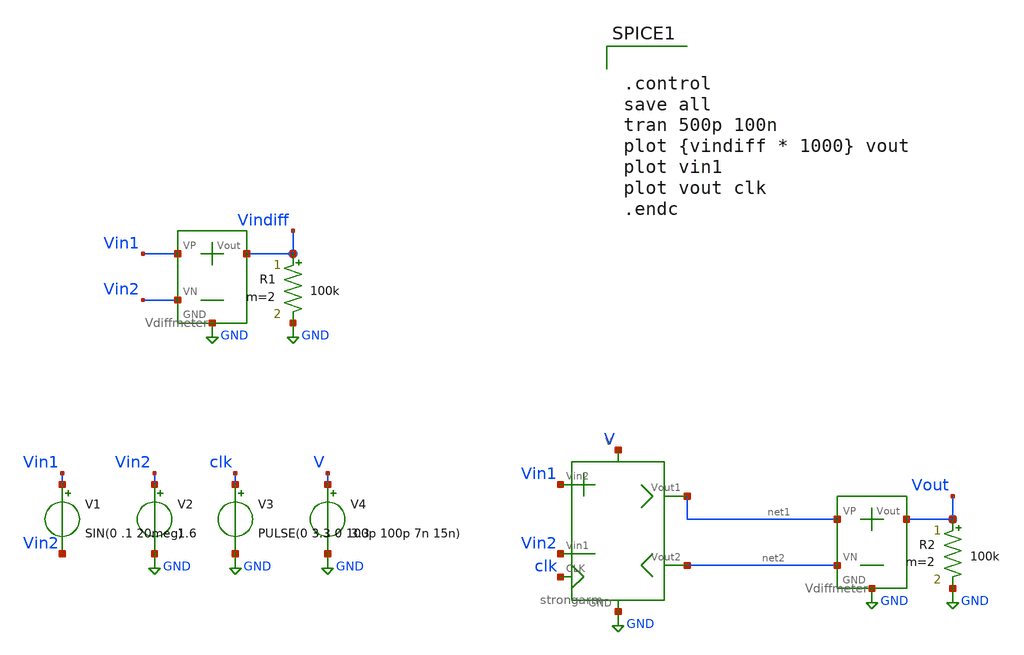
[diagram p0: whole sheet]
** sch_path: SAR_ADC/xschem/test/strongarm_tb/sin_1m__tb.sch
**.subckt sin_1m__tb
V1 Vin1 Vin2 SIN(0 .1 20meg)
V2 Vin2 GND 1.6
V3 clk GND PULSE(0 3.3 0 100p 100p 7n 15n)
V4 V GND 3.3
R1 Vindiff GND 100k m=2
R2 Vout GND 100k m=2
X1 V GND Vin2 Vin1 clk net1 net2 strongarm
X3 net1 net2 Vout GND Vdiffmeter
X2 Vin1 Vin2 Vindiff GND Vdiffmeter
**** begin user architecture code


.control
save all
tran 500p 100n
plot {vindiff * 1000} vout
plot vin1
plot vout clk
.endc


.include $::PDK_ROOT/gf180mcuC/libs.tech/ngspice/design.ngspice
.lib $::PDK_ROOT/gf180mcuC/libs.tech/ngspice/sm141064.ngspice typical

**** end user architecture code
**.ends

* expanding   symbol:  ../../../symbols/strongarm.sym # of pins=7
** sym_path: SAR_ADC/xschem/designs/strongarm.sym
** sch_path: SAR_ADC/xschem/designs/strongarm.sch
.subckt strongarm V GND Vin1 Vin2 CLK Vout1 Vout2
*.iopin V
*.iopin Vout1
*.iopin Vin1
*.iopin Vin2
*.iopin Vout2
*.iopin CLK
*.iopin GND
XM1 net3 Vout2 V V pfet_03v3 L=0.28u W=2u nf=1 ad='int((nf+1)/2) * W/nf * 0.18u' as='int((nf+2)/2) * W/nf * 0.18u'
+ pd='2*int((nf+1)/2) * (W/nf + 0.18u)' ps='2*int((nf+2)/2) * (W/nf + 0.18u)' nrd='0.18u / W' nrs='0.18u / W'
+ sa=0 sb=0 sd=0 m=1
XM2 Vout1 net1 GND GND nfet_03v3 L=0.28u W=2u nf=1 ad='int((nf+1)/2) * W/nf * 0.18u' as='int((nf+2)/2) * W/nf * 0.18u'
+ pd='2*int((nf+1)/2) * (W/nf + 0.18u)' ps='2*int((nf+2)/2) * (W/nf + 0.18u)' nrd='0.18u / W' nrs='0.18u / W'
+ sa=0 sb=0 sd=0 m=1
XM3 Vout2 Vout1 GND GND nfet_03v3 L=0.28u W=2u nf=1 ad='int((nf+1)/2) * W/nf * 0.18u' as='int((nf+2)/2) * W/nf * 0.18u'
+ pd='2*int((nf+1)/2) * (W/nf + 0.18u)' ps='2*int((nf+2)/2) * (W/nf + 0.18u)' nrd='0.18u / W' nrs='0.18u / W'
+ sa=0 sb=0 sd=0 m=1
XM4 Vout2 net1 GND GND nfet_03v3 L=0.28u W=2u nf=1 ad='int((nf+1)/2) * W/nf * 0.18u' as='int((nf+2)/2) * W/nf * 0.18u'
+ pd='2*int((nf+1)/2) * (W/nf + 0.18u)' ps='2*int((nf+2)/2) * (W/nf + 0.18u)' nrd='0.18u / W' nrs='0.18u / W'
+ sa=0 sb=0 sd=0 m=1
XM5 Vout1 Vout2 GND GND nfet_03v3 L=0.28u W=2u nf=1 ad='int((nf+1)/2) * W/nf * 0.18u' as='int((nf+2)/2) * W/nf * 0.18u'
+ pd='2*int((nf+1)/2) * (W/nf + 0.18u)' ps='2*int((nf+2)/2) * (W/nf + 0.18u)' nrd='0.18u / W' nrs='0.18u / W'
+ sa=0 sb=0 sd=0 m=1
XM6 net2 Vout1 V V pfet_03v3 L=0.28u W=2u nf=1 ad='int((nf+1)/2) * W/nf * 0.18u' as='int((nf+2)/2) * W/nf * 0.18u'
+ pd='2*int((nf+1)/2) * (W/nf + 0.18u)' ps='2*int((nf+2)/2) * (W/nf + 0.18u)' nrd='0.18u / W' nrs='0.18u / W'
+ sa=0 sb=0 sd=0 m=1
XM7 Vout1 Vin1 net3 V pfet_03v3 L=0.28u W=10u nf=1 ad='int((nf+1)/2) * W/nf * 0.18u' as='int((nf+2)/2) * W/nf * 0.18u'
+ pd='2*int((nf+1)/2) * (W/nf + 0.18u)' ps='2*int((nf+2)/2) * (W/nf + 0.18u)' nrd='0.18u / W' nrs='0.18u / W'
+ sa=0 sb=0 sd=0 m=1
XM8 Vout2 Vin2 net2 V pfet_03v3 L=0.28u W=10u nf=1 ad='int((nf+1)/2) * W/nf * 0.18u' as='int((nf+2)/2) * W/nf * 0.18u'
+ pd='2*int((nf+1)/2) * (W/nf + 0.18u)' ps='2*int((nf+2)/2) * (W/nf + 0.18u)' nrd='0.18u / W' nrs='0.18u / W'
+ sa=0 sb=0 sd=0 m=1
x1 V GND net4 CLK inv cl=0.28u wp=0.44u wn=0.22u wx=4u
x2 V GND net1 net4 inv cl=0.28u wp=0.44u wn=0.22u wx=4u
.ends


* expanding   symbol:  ../../../symbols/Vdiffmeter.sym # of pins=4
** sym_path: SAR_ADC/xschem/spice/symbols/Vdiffmeter.sym
** sch_path: SAR_ADC/xschem/spice/symbols/Vdiffmeter.sch
.subckt Vdiffmeter VP VN Vout GND
*.iopin Vout
*.iopin GND
*.iopin VP
*.iopin VN
R4 Vout GND 1k m=1
E4 Vout GND VP VN 1
.ends


* expanding   symbol:  inv.sym # of pins=4
** sym_path: SAR_ADC/xschem/designs/inv.sym
** sch_path: SAR_ADC/xschem/designs/inv.sch
.subckt inv vdd gnd vout vin  cl=0.28u wp=0.44u wn=0.22u wx=0.22u
*.ipin gnd
*.ipin vdd
*.ipin vin
*.opin vout
XM1 gnd vin vout gnd nfet_03v3 L=0.28u W=8u nf=1 ad='int((nf+1)/2) * W/nf * 0.18u' as='int((nf+2)/2) * W/nf * 0.18u'
+ pd='2*int((nf+1)/2) * (W/nf + 0.18u)' ps='2*int((nf+2)/2) * (W/nf + 0.18u)' nrd='0.18u / W' nrs='0.18u / W'
+ sa=0 sb=0 sd=0 m=1
XM2 vdd vin vout vdd pfet_03v3 L=0.28u W=8u nf=1 ad='int((nf+1)/2) * W/nf * 0.18u' as='int((nf+2)/2) * W/nf * 0.18u'
+ pd='2*int((nf+1)/2) * (W/nf + 0.18u)' ps='2*int((nf+2)/2) * (W/nf + 0.18u)' nrd='0.18u / W' nrs='0.18u / W'
+ sa=0 sb=0 sd=0 m=1
.ends

.GLOBAL GND
.end
